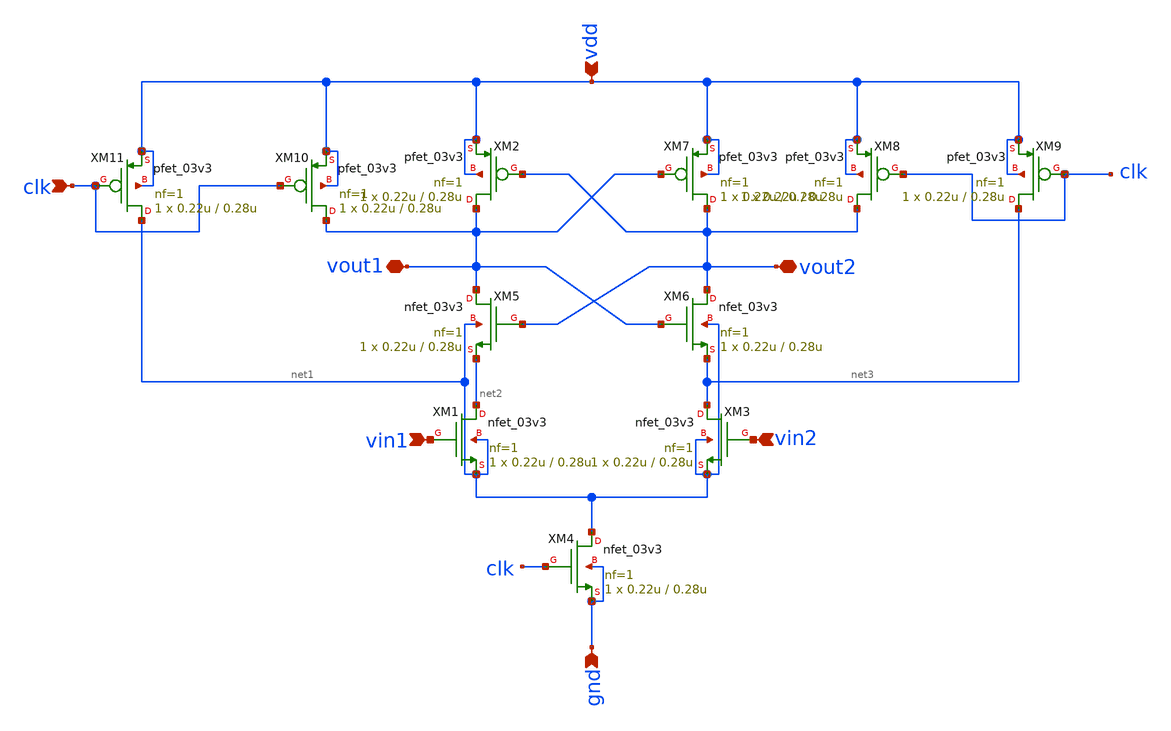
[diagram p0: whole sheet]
** sch_path: designs/DS_modulator/comparator/xschem/schematic.sch
**.subckt schematic vin1 vin2 clk vdd vout2 vout1 gnd
*.ipin vin1
*.ipin vin2
*.ipin clk
*.ipin vdd
*.iopin vout2
*.iopin vout1
*.ipin gnd
XM1 net2 vin1 net1 net1 nfet_03v3 L=0.28u W=0.22u nf=1 ad='int((nf+1)/2) * W/nf * 0.18u' as='int((nf+2)/2) * W/nf * 0.18u'
+ pd='2*int((nf+1)/2) * (W/nf + 0.18u)' ps='2*int((nf+2)/2) * (W/nf + 0.18u)' nrd='0.18u / W' nrs='0.18u / W'
+ sa=0 sb=0 sd=0 m=1
XM2 vout1 vout2 vdd vdd pfet_03v3 L=0.28u W=0.22u nf=1 ad='int((nf+1)/2) * W/nf * 0.18u' as='int((nf+2)/2) * W/nf * 0.18u'
+ pd='2*int((nf+1)/2) * (W/nf + 0.18u)' ps='2*int((nf+2)/2) * (W/nf + 0.18u)' nrd='0.18u / W' nrs='0.18u / W'
+ sa=0 sb=0 sd=0 m=1
XM3 net3 vin2 net1 net1 nfet_03v3 L=0.28u W=0.22u nf=1 ad='int((nf+1)/2) * W/nf * 0.18u' as='int((nf+2)/2) * W/nf * 0.18u'
+ pd='2*int((nf+1)/2) * (W/nf + 0.18u)' ps='2*int((nf+2)/2) * (W/nf + 0.18u)' nrd='0.18u / W' nrs='0.18u / W'
+ sa=0 sb=0 sd=0 m=1
XM4 net1 clk gnd gnd nfet_03v3 L=0.28u W=0.22u nf=1 ad='int((nf+1)/2) * W/nf * 0.18u' as='int((nf+2)/2) * W/nf * 0.18u'
+ pd='2*int((nf+1)/2) * (W/nf + 0.18u)' ps='2*int((nf+2)/2) * (W/nf + 0.18u)' nrd='0.18u / W' nrs='0.18u / W'
+ sa=0 sb=0 sd=0 m=1
XM5 vout1 vout2 net2 net1 nfet_03v3 L=0.28u W=0.22u nf=1 ad='int((nf+1)/2) * W/nf * 0.18u' as='int((nf+2)/2) * W/nf * 0.18u'
+ pd='2*int((nf+1)/2) * (W/nf + 0.18u)' ps='2*int((nf+2)/2) * (W/nf + 0.18u)' nrd='0.18u / W' nrs='0.18u / W'
+ sa=0 sb=0 sd=0 m=1
XM6 vout2 vout1 net3 net1 nfet_03v3 L=0.28u W=0.22u nf=1 ad='int((nf+1)/2) * W/nf * 0.18u' as='int((nf+2)/2) * W/nf * 0.18u'
+ pd='2*int((nf+1)/2) * (W/nf + 0.18u)' ps='2*int((nf+2)/2) * (W/nf + 0.18u)' nrd='0.18u / W' nrs='0.18u / W'
+ sa=0 sb=0 sd=0 m=1
XM7 vout2 vout1 vdd vdd pfet_03v3 L=0.28u W=0.22u nf=1 ad='int((nf+1)/2) * W/nf * 0.18u' as='int((nf+2)/2) * W/nf * 0.18u'
+ pd='2*int((nf+1)/2) * (W/nf + 0.18u)' ps='2*int((nf+2)/2) * (W/nf + 0.18u)' nrd='0.18u / W' nrs='0.18u / W'
+ sa=0 sb=0 sd=0 m=1
XM8 vout2 clk vdd vdd pfet_03v3 L=0.28u W=0.22u nf=1 ad='int((nf+1)/2) * W/nf * 0.18u' as='int((nf+2)/2) * W/nf * 0.18u'
+ pd='2*int((nf+1)/2) * (W/nf + 0.18u)' ps='2*int((nf+2)/2) * (W/nf + 0.18u)' nrd='0.18u / W' nrs='0.18u / W'
+ sa=0 sb=0 sd=0 m=1
XM9 net3 clk vdd vdd pfet_03v3 L=0.28u W=0.22u nf=1 ad='int((nf+1)/2) * W/nf * 0.18u' as='int((nf+2)/2) * W/nf * 0.18u'
+ pd='2*int((nf+1)/2) * (W/nf + 0.18u)' ps='2*int((nf+2)/2) * (W/nf + 0.18u)' nrd='0.18u / W' nrs='0.18u / W'
+ sa=0 sb=0 sd=0 m=1
XM10 vout1 clk vdd vdd pfet_03v3 L=0.28u W=0.22u nf=1 ad='int((nf+1)/2) * W/nf * 0.18u' as='int((nf+2)/2) * W/nf * 0.18u'
+ pd='2*int((nf+1)/2) * (W/nf + 0.18u)' ps='2*int((nf+2)/2) * (W/nf + 0.18u)' nrd='0.18u / W' nrs='0.18u / W'
+ sa=0 sb=0 sd=0 m=1
XM11 net1 clk vdd vdd pfet_03v3 L=0.28u W=0.22u nf=1 ad='int((nf+1)/2) * W/nf * 0.18u' as='int((nf+2)/2) * W/nf * 0.18u'
+ pd='2*int((nf+1)/2) * (W/nf + 0.18u)' ps='2*int((nf+2)/2) * (W/nf + 0.18u)' nrd='0.18u / W' nrs='0.18u / W'
+ sa=0 sb=0 sd=0 m=1
**.ends
.end
